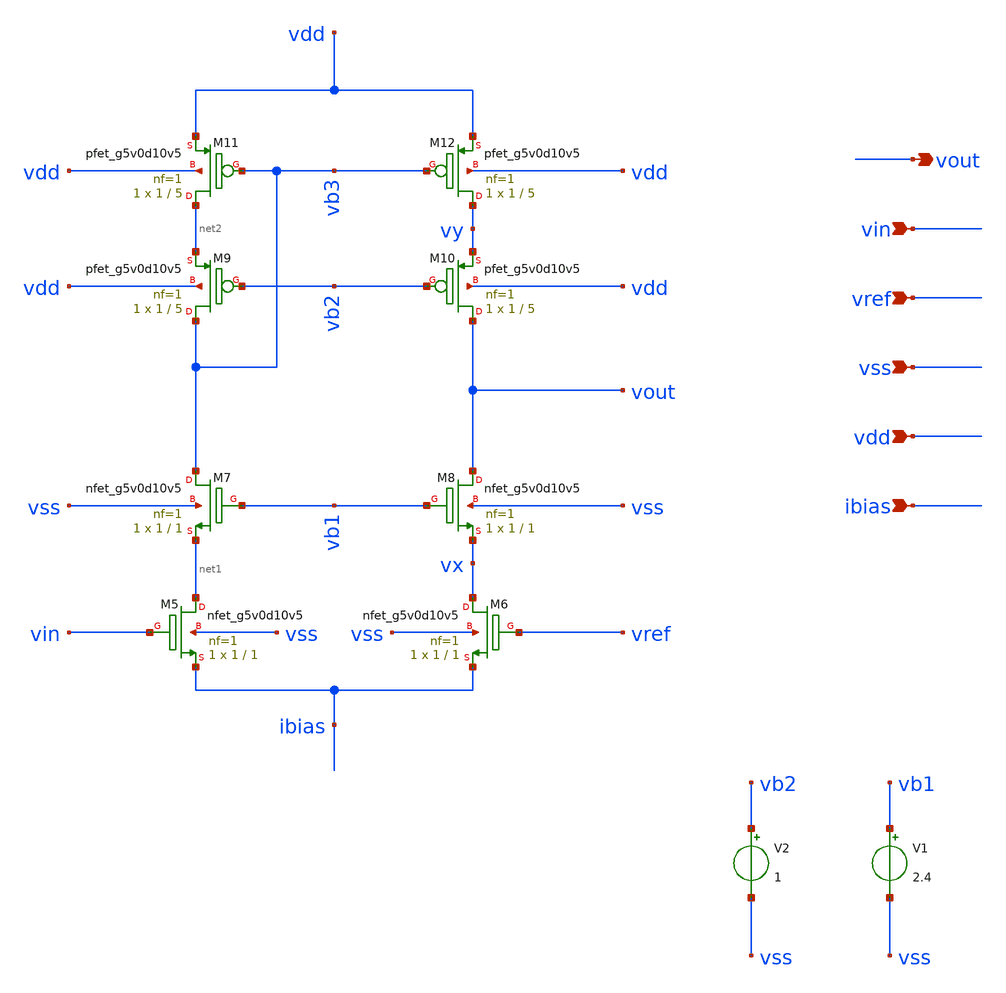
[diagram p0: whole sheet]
** sch_path: xschem/cascode_opamp.sch
**.subckt cascode_opamp vin vref vss vout vdd ibias
*.ipin vin
*.ipin vref
*.ipin vss
*.opin vout
*.ipin vdd
*.ipin ibias
XM5 net1 vin ibias vss sky130_fd_pr__nfet_g5v0d10v5 L=1 W=1 nf=1 ad='int((nf+1)/2) * W/nf * 0.29' as='int((nf+2)/2) * W/nf * 0.29'
+ pd='2*int((nf+1)/2) * (W/nf + 0.29)' ps='2*int((nf+2)/2) * (W/nf + 0.29)' nrd='0.29 / W' nrs='0.29 / W'
+ sa=0 sb=0 sd=0 mult=1 m=1
XM6 vx vref ibias vss sky130_fd_pr__nfet_g5v0d10v5 L=1 W=1 nf=1 ad='int((nf+1)/2) * W/nf * 0.29' as='int((nf+2)/2) * W/nf * 0.29'
+ pd='2*int((nf+1)/2) * (W/nf + 0.29)' ps='2*int((nf+2)/2) * (W/nf + 0.29)' nrd='0.29 / W' nrs='0.29 / W'
+ sa=0 sb=0 sd=0 mult=1 m=1
XM7 vb3 vb1 net1 vss sky130_fd_pr__nfet_g5v0d10v5 L=1 W=1 nf=1 ad='int((nf+1)/2) * W/nf * 0.29' as='int((nf+2)/2) * W/nf * 0.29'
+ pd='2*int((nf+1)/2) * (W/nf + 0.29)' ps='2*int((nf+2)/2) * (W/nf + 0.29)' nrd='0.29 / W' nrs='0.29 / W'
+ sa=0 sb=0 sd=0 mult=1 m=1
XM8 vout vb1 vx vss sky130_fd_pr__nfet_g5v0d10v5 L=1 W=1 nf=1 ad='int((nf+1)/2) * W/nf * 0.29' as='int((nf+2)/2) * W/nf * 0.29'
+ pd='2*int((nf+1)/2) * (W/nf + 0.29)' ps='2*int((nf+2)/2) * (W/nf + 0.29)' nrd='0.29 / W' nrs='0.29 / W'
+ sa=0 sb=0 sd=0 mult=1 m=1
XM9 vb3 vb2 net2 vdd sky130_fd_pr__pfet_g5v0d10v5 L=5 W=1 nf=1 ad='int((nf+1)/2) * W/nf * 0.29' as='int((nf+2)/2) * W/nf * 0.29'
+ pd='2*int((nf+1)/2) * (W/nf + 0.29)' ps='2*int((nf+2)/2) * (W/nf + 0.29)' nrd='0.29 / W' nrs='0.29 / W'
+ sa=0 sb=0 sd=0 mult=1 m=1
XM10 vout vb2 vy vdd sky130_fd_pr__pfet_g5v0d10v5 L=5 W=1 nf=1 ad='int((nf+1)/2) * W/nf * 0.29' as='int((nf+2)/2) * W/nf * 0.29'
+ pd='2*int((nf+1)/2) * (W/nf + 0.29)' ps='2*int((nf+2)/2) * (W/nf + 0.29)' nrd='0.29 / W' nrs='0.29 / W'
+ sa=0 sb=0 sd=0 mult=1 m=1
XM11 net2 vb3 vdd vdd sky130_fd_pr__pfet_g5v0d10v5 L=5 W=1 nf=1 ad='int((nf+1)/2) * W/nf * 0.29' as='int((nf+2)/2) * W/nf * 0.29'
+ pd='2*int((nf+1)/2) * (W/nf + 0.29)' ps='2*int((nf+2)/2) * (W/nf + 0.29)' nrd='0.29 / W' nrs='0.29 / W'
+ sa=0 sb=0 sd=0 mult=1 m=1
XM12 vy vb3 vdd vdd sky130_fd_pr__pfet_g5v0d10v5 L=5 W=1 nf=1 ad='int((nf+1)/2) * W/nf * 0.29' as='int((nf+2)/2) * W/nf * 0.29'
+ pd='2*int((nf+1)/2) * (W/nf + 0.29)' ps='2*int((nf+2)/2) * (W/nf + 0.29)' nrd='0.29 / W' nrs='0.29 / W'
+ sa=0 sb=0 sd=0 mult=1 m=1
V1 vb1 vss 2.4
V2 vb2 vss 1
**.ends
.end
